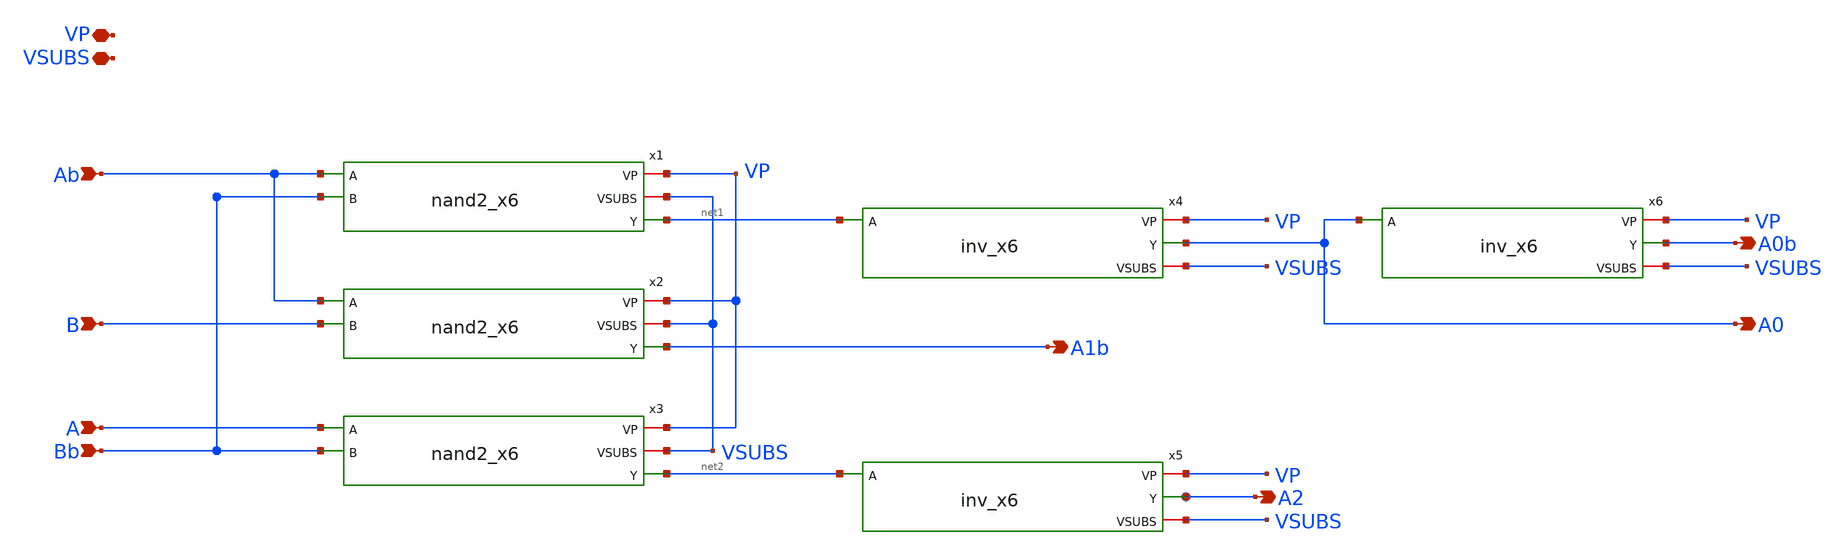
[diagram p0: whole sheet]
** sch_path: xschem/decoder2to4_x6.sch
**.subckt decoder2to4_x6 A0 A1b A2 VP VSUBS Ab B A Bb A0b
*.opin A0
*.opin A1b
*.opin A2
*.iopin VP
*.iopin VSUBS
*.ipin Ab
*.ipin B
*.ipin A
*.ipin Bb
*.opin A0b
x4 VP net1 A0 VSUBS inv_x6
x5 VP net2 A2 VSUBS inv_x6
x6 VP A0 A0b VSUBS inv_x6
x1 VP VSUBS Ab Bb net1 nand2_x6
x2 VP VSUBS Ab B A1b nand2_x6
x3 VP VSUBS A Bb net2 nand2_x6
**.ends

* expanding   symbol:  inv_x6.sym # of pins=4
** sym_path: xschem/inv_x6.sym
** sch_path: xschem/inv_x6.sch
.subckt inv_x6 VP A Y VSUBS
*.iopin VP
*.iopin VSUBS
*.ipin A
*.opin Y
XM1 Y A VSUBS VSUBS sky130_fd_pr__nfet_g5v0d10v5 L=0.5 W=1 nf=1 ad='int((nf+1)/2) * W/nf * 0.29' as='int((nf+2)/2) * W/nf * 0.29'
+ pd='2*int((nf+1)/2) * (W/nf + 0.29)' ps='2*int((nf+2)/2) * (W/nf + 0.29)' nrd='0.29 / W' nrs='0.29 / W'
+ sa=0 sb=0 sd=0 mult=4 m=4
XM2 Y A VP VP sky130_fd_pr__pfet_g5v0d10v5 L=0.5 W=1 nf=1 ad='int((nf+1)/2) * W/nf * 0.29' as='int((nf+2)/2) * W/nf * 0.29'
+ pd='2*int((nf+1)/2) * (W/nf + 0.29)' ps='2*int((nf+2)/2) * (W/nf + 0.29)' nrd='0.29 / W' nrs='0.29 / W'
+ sa=0 sb=0 sd=0 mult=6 m=6
.ends


* expanding   symbol:  nand2_x6.sym # of pins=5
** sym_path: xschem/nand2_x6.sym
** sch_path: xschem/nand2_x6.sch
.subckt nand2_x6 VP VSUBS A B Y
*.iopin VP
*.iopin VSUBS
*.ipin A
*.ipin B
*.opin Y
XM1 Y B net1 VSUBS sky130_fd_pr__nfet_g5v0d10v5 L=0.5 W=1 nf=1 ad='int((nf+1)/2) * W/nf * 0.29' as='int((nf+2)/2) * W/nf * 0.29'
+ pd='2*int((nf+1)/2) * (W/nf + 0.29)' ps='2*int((nf+2)/2) * (W/nf + 0.29)' nrd='0.29 / W' nrs='0.29 / W'
+ sa=0 sb=0 sd=0 mult=4 m=4
XM2 net1 A VSUBS VSUBS sky130_fd_pr__nfet_g5v0d10v5 L=0.5 W=1 nf=1 ad='int((nf+1)/2) * W/nf * 0.29' as='int((nf+2)/2) * W/nf * 0.29'
+ pd='2*int((nf+1)/2) * (W/nf + 0.29)' ps='2*int((nf+2)/2) * (W/nf + 0.29)' nrd='0.29 / W' nrs='0.29 / W'
+ sa=0 sb=0 sd=0 mult=4 m=4
XM3 Y A VP VP sky130_fd_pr__pfet_g5v0d10v5 L=0.5 W=1 nf=1 ad='int((nf+1)/2) * W/nf * 0.29' as='int((nf+2)/2) * W/nf * 0.29'
+ pd='2*int((nf+1)/2) * (W/nf + 0.29)' ps='2*int((nf+2)/2) * (W/nf + 0.29)' nrd='0.29 / W' nrs='0.29 / W'
+ sa=0 sb=0 sd=0 mult=6 m=6
XM4 Y B VP VP sky130_fd_pr__pfet_g5v0d10v5 L=0.5 W=1 nf=1 ad='int((nf+1)/2) * W/nf * 0.29' as='int((nf+2)/2) * W/nf * 0.29'
+ pd='2*int((nf+1)/2) * (W/nf + 0.29)' ps='2*int((nf+2)/2) * (W/nf + 0.29)' nrd='0.29 / W' nrs='0.29 / W'
+ sa=0 sb=0 sd=0 mult=6 m=6
.ends

.end
